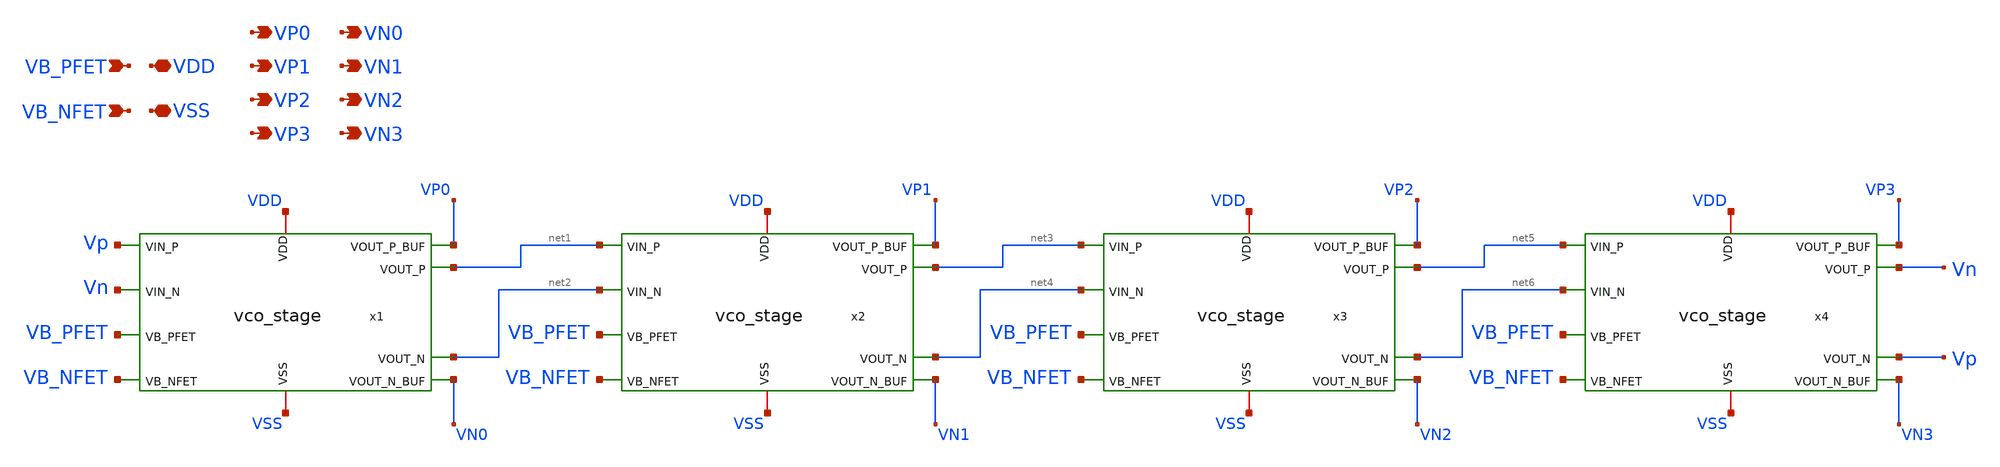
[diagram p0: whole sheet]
** sch_path: xschem/vco_core.sch
**.subckt vco_core VDD VSS VB_PFET VB_NFET VP0 VP1 VP2 VP3 VN0 VN1 VN2 VN3
*.iopin VDD
*.iopin VSS
*.ipin VB_PFET
*.ipin VB_NFET
*.opin VP0
*.opin VP1
*.opin VP2
*.opin VP3
*.opin VN0
*.opin VN1
*.opin VN2
*.opin VN3
x1 VDD VSS Vp Vn VB_PFET VB_NFET net1 net2 VP0 VN0 vco_stage
x2 VDD VSS net1 net2 VB_PFET VB_NFET net3 net4 VP1 VN1 vco_stage
x3 VDD VSS net3 net4 VB_PFET VB_NFET net5 net6 VP2 VN2 vco_stage
x4 VDD VSS net5 net6 VB_PFET VB_NFET Vn Vp VP3 VN3 vco_stage
**.ends

* expanding   symbol:  vco_stage.sym # of pins=10
** sym_path: xschem/vco_stage.sym
** sch_path: xschem/vco_stage.sch
.subckt vco_stage VDD VSS VIN_P VIN_N VB_PFET VB_NFET VOUT_P VOUT_N VOUT_P_BUF VOUT_N_BUF
*.iopin VDD
*.iopin VSS
*.ipin VIN_P
*.ipin VIN_N
*.ipin VB_PFET
*.ipin VB_NFET
*.opin VOUT_P
*.opin VOUT_N
*.opin VOUT_P_BUF
*.opin VOUT_N_BUF
x1 VDD VSS VIN_P VB_PFET VOUT_N VOUT_P VDRAIN_M5 VOUT_P_BUF vco_stage_half
x2 VDD VSS VIN_N VB_PFET VOUT_P VOUT_N VDRAIN_M5 VOUT_N_BUF vco_stage_half
XM5 VDRAIN_M5 VB_NFET VSS VSS sky130_fd_pr__nfet_01v8 L=2 W=4 nf=2 ad='int((nf+1)/2) * W/nf * 0.29' as='int((nf+2)/2) * W/nf * 0.29'
+ pd='2*int((nf+1)/2) * (W/nf + 0.29)' ps='2*int((nf+2)/2) * (W/nf + 0.29)' nrd='0.29 / W' nrs='0.29 / W'
+ sa=0 sb=0 sd=0 mult=1 m=1
.ends


* expanding   symbol:  vco_stage_half.sym # of pins=8
** sym_path: xschem/vco_stage_half.sym
** sch_path: xschem/vco_stage_half.sch
.subckt vco_stage_half VDD VSS VIN_DIFF VB_PFET VFB VOUT_DIFF VDRAIN_TAIL VOUT_DIFF_BUF
*.iopin VDD
*.iopin VSS
*.ipin VIN_DIFF
*.ipin VB_PFET
*.ipin VFB
*.opin VOUT_DIFF
*.opin VDRAIN_TAIL
*.opin VOUT_DIFF_BUF
XM7 VOUT_DIFF VFB VDD VDD sky130_fd_pr__pfet_01v8 L=2 W=4 nf=2 ad='int((nf+1)/2) * W/nf * 0.29' as='int((nf+2)/2) * W/nf * 0.29'
+ pd='2*int((nf+1)/2) * (W/nf + 0.29)' ps='2*int((nf+2)/2) * (W/nf + 0.29)' nrd='0.29 / W' nrs='0.29 / W'
+ sa=0 sb=0 sd=0 mult=1 m=1
XM3 VOUT_DIFF VB_PFET VDD VDD sky130_fd_pr__pfet_01v8 L=2 W=4 nf=2 ad='int((nf+1)/2) * W/nf * 0.29' as='int((nf+2)/2) * W/nf * 0.29'
+ pd='2*int((nf+1)/2) * (W/nf + 0.29)' ps='2*int((nf+2)/2) * (W/nf + 0.29)' nrd='0.29 / W' nrs='0.29 / W'
+ sa=0 sb=0 sd=0 mult=1 m=1
XM1 VOUT_DIFF VIN_DIFF VDRAIN_TAIL VSS sky130_fd_pr__nfet_01v8 L=2 W=4 nf=2 ad='int((nf+1)/2) * W/nf * 0.29'
+ as='int((nf+2)/2) * W/nf * 0.29' pd='2*int((nf+1)/2) * (W/nf + 0.29)' ps='2*int((nf+2)/2) * (W/nf + 0.29)'
+ nrd='0.29 / W' nrs='0.29 / W' sa=0 sb=0 sd=0 mult=1 m=1
x1 VDD VSS VOUT_DIFF VOUT_DIFF_BUF vco_buffer
XM8 VSS VOUT_DIFF VSS VSS sky130_fd_pr__nfet_01v8 L=11 W=11 nf=1 ad='int((nf+1)/2) * W/nf * 0.29' as='int((nf+2)/2) * W/nf * 0.29'
+ pd='2*int((nf+1)/2) * (W/nf + 0.29)' ps='2*int((nf+2)/2) * (W/nf + 0.29)' nrd='0.29 / W' nrs='0.29 / W'
+ sa=0 sb=0 sd=0 mult=1 m=1
.ends


* expanding   symbol:  vco_buffer.sym # of pins=4
** sym_path: xschem/vco_buffer.sym
** sch_path: xschem/vco_buffer.sch
.subckt vco_buffer VDD VSS VIN_BUF VOUT_BUF
*.iopin VDD
*.iopin VSS
*.ipin VIN_BUF
*.opin VOUT_BUF
x1 VDD VIN_BUF INT_BUF VSS vco_inverter
x2 VDD INT_BUF VOUT_BUF VSS vco_inverter
.ends


* expanding   symbol:  vco_inverter.sym # of pins=4
** sym_path: xschem/vco_inverter.sym
** sch_path: xschem/vco_inverter.sch
.subckt vco_inverter VDD VIN_INV VOUT_INV VSS
*.iopin VDD
*.iopin VSS
*.ipin VIN_INV
*.opin VOUT_INV
XM1 VOUT_INV VIN_INV VSS VSS sky130_fd_pr__nfet_01v8 L=0.15 W=1 nf=1 ad='int((nf+1)/2) * W/nf * 0.29'
+ as='int((nf+2)/2) * W/nf * 0.29' pd='2*int((nf+1)/2) * (W/nf + 0.29)' ps='2*int((nf+2)/2) * (W/nf + 0.29)'
+ nrd='0.29 / W' nrs='0.29 / W' sa=0 sb=0 sd=0 mult=1 m=1
XM2 VOUT_INV VIN_INV VDD VDD sky130_fd_pr__pfet_01v8 L=0.15 W=1 nf=1 ad='int((nf+1)/2) * W/nf * 0.29'
+ as='int((nf+2)/2) * W/nf * 0.29' pd='2*int((nf+1)/2) * (W/nf + 0.29)' ps='2*int((nf+2)/2) * (W/nf + 0.29)'
+ nrd='0.29 / W' nrs='0.29 / W' sa=0 sb=0 sd=0 mult=1 m=1
.ends

.end
